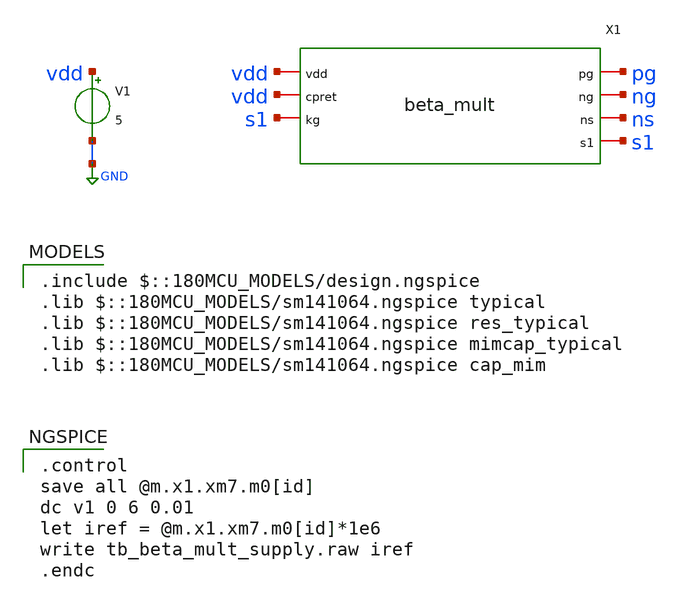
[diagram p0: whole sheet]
** sch_path: schematic pt2/sims/tb/tb_beta_mult_supply.sch
**.subckt tb_beta_mult_supply
V1 vdd GND 5
X1 vdd pg ng ns vdd s1 s1 beta_mult
**** begin user architecture code
 .include $::180MCU_MODELS/design.ngspice
.lib $::180MCU_MODELS/sm141064.ngspice typical
.lib $::180MCU_MODELS/sm141064.ngspice res_typical
.lib $::180MCU_MODELS/sm141064.ngspice mimcap_typical
.lib $::180MCU_MODELS/sm141064.ngspice cap_mim

.control
save all @m.x1.xm7.m0[id]
dc v1 0 6 0.01
let iref = @m.x1.xm7.m0[id]*1e6
write tb_beta_mult_supply.raw iref
.endc

**** end user architecture code
**.ends
.GLOBAL GND
.end
